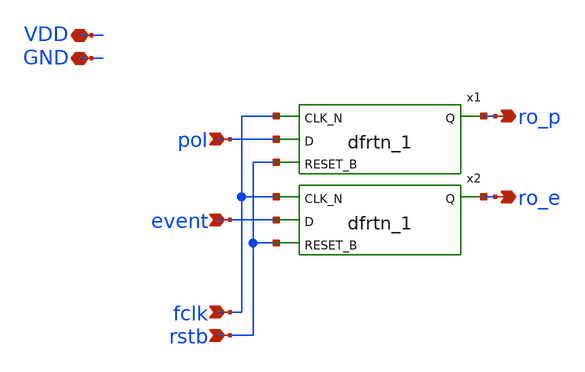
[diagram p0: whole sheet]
** sch_path: xschem/readout/ro_cell.sch
**.subckt ro_cell pol event fclk rstb VDD GND ro_p ro_e
*.ipin pol
*.ipin event
*.ipin fclk
*.ipin rstb
*.iopin VDD
*.iopin GND
*.opin ro_p
*.opin ro_e
x1 fclk pol rstb GND GND VDD VDD ro_p sky130_fd_sc_lp__dfrtn_1
x2 fclk event rstb GND GND VDD VDD ro_e sky130_fd_sc_lp__dfrtn_1
**.ends
.end
